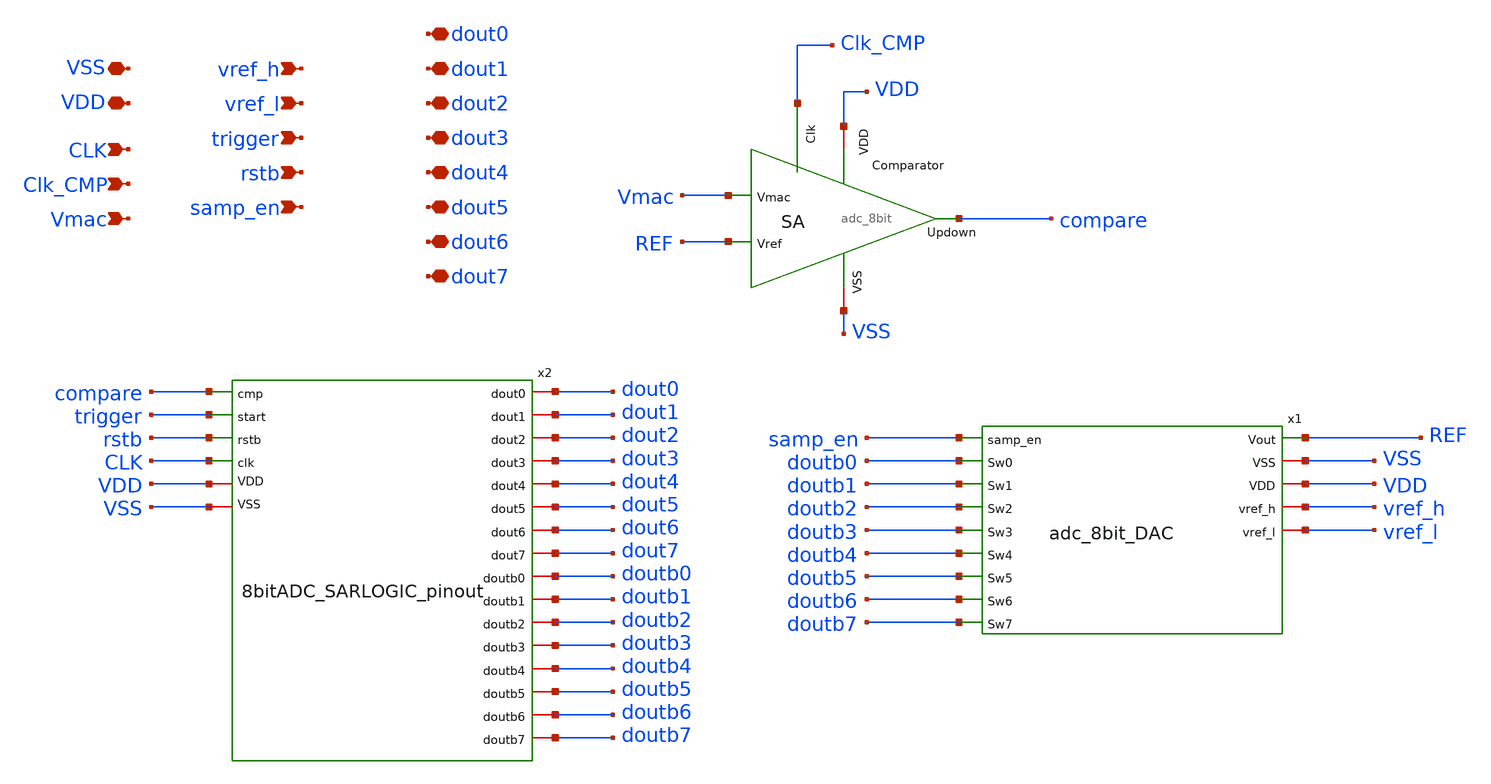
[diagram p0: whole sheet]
** sch_path: ADC.sch
**.subckt ADC vref_l CLK Clk_CMP Vmac vref_h trigger rstb samp_en dout0 VSS VDD dout1 dout2 dout3
*+ dout4 dout5 dout6 dout7
*.ipin vref_l
*.ipin CLK
*.ipin Clk_CMP
*.ipin Vmac
*.ipin vref_h
*.ipin trigger
*.ipin rstb
*.ipin samp_en
*.iopin dout0
*.iopin VSS
*.iopin VDD
*.iopin dout1
*.iopin dout2
*.iopin dout3
*.iopin dout4
*.iopin dout5
*.iopin dout6
*.iopin dout7
x1 REF VSS samp_en doutb0 VDD doutb1 vref_h doutb2 vref_l doutb3 doutb4 doutb5 doutb6 doutb7
+ adc_8bit_DAC
x3 VSS VDD REF Clk_CMP Vmac compare adc_8bit
x2 VDD compare VSS trigger doutb0 dout0 rstb CLK doutb1 dout1 doutb2 dout2 dout3 doutb3 dout4 doutb4
+ dout5 doutb5 dout6 doutb6 doutb7 dout7 8bitADC_SARLOGIC_pinout
**.ends
.end
